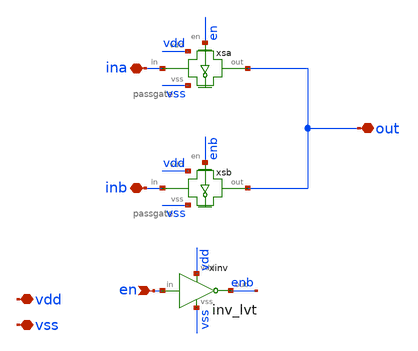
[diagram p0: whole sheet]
** sch_path: xschem/support/spdt.sch
**.subckt spdt en vss vdd ina out inb
*.ipin en
*.iopin vss
*.iopin vdd
*.iopin ina
*.iopin out
*.iopin inb
xinv vdd en enb vss inv_lvt
xsa out en vdd ina vss passgate
xsb out enb vdd inb vss passgate
**.ends

* expanding   symbol:  logic/inv_lvt.sym # of pins=4
** sym_path: xschem/logic/inv_lvt.sym
** sch_path: xschem/logic/inv_lvt.sch
.subckt inv_lvt vdd in out vss
*.iopin vdd
*.iopin vss
*.ipin in
*.opin out
XM1 out in vss vss sky130_fd_pr__nfet_01v8_lvt L=0.4 W=1 nf=1 ad='int((nf+1)/2) * W/nf * 0.29' as='int((nf+2)/2) * W/nf * 0.29'
+ pd='2*int((nf+1)/2) * (W/nf + 0.29)' ps='2*int((nf+2)/2) * (W/nf + 0.29)' nrd='0.29 / W' nrs='0.29 / W'
+ sa=0 sb=0 sd=0 mult=1 m=1
XM2 out in vdd vdd sky130_fd_pr__pfet_01v8_lvt L=0.4 W=1 nf=1 ad='int((nf+1)/2) * W/nf * 0.29' as='int((nf+2)/2) * W/nf * 0.29'
+ pd='2*int((nf+1)/2) * (W/nf + 0.29)' ps='2*int((nf+2)/2) * (W/nf + 0.29)' nrd='0.29 / W' nrs='0.29 / W'
+ sa=0 sb=0 sd=0 mult=1 m=1
.ends


* expanding   symbol:  switches/passgate.sym # of pins=5
** sym_path: xschem/switches/passgate.sym
** sch_path: xschem/switches/passgate.sch
.subckt passgate out en vdd in vss
*.iopin out
*.ipin en
*.iopin vss
*.iopin vdd
*.iopin in
x2 vdd en enb vss inv_lvt
x1 vdd enb en_buf vss inv_lvt
XMSN out en_buf in vss sky130_fd_pr__nfet_01v8 L=0.5 W=1 nf=1 ad='int((nf+1)/2) * W/nf * 0.29' as='int((nf+2)/2) * W/nf * 0.29'
+ pd='2*int((nf+1)/2) * (W/nf + 0.29)' ps='2*int((nf+2)/2) * (W/nf + 0.29)' nrd='0.29 / W' nrs='0.29 / W'
+ sa=0 sb=0 sd=0 mult=1 m=1
XMSP in enb out vdd sky130_fd_pr__pfet_01v8 L=0.5 W=1 nf=1 ad='int((nf+1)/2) * W/nf * 0.29' as='int((nf+2)/2) * W/nf * 0.29'
+ pd='2*int((nf+1)/2) * (W/nf + 0.29)' ps='2*int((nf+2)/2) * (W/nf + 0.29)' nrd='0.29 / W' nrs='0.29 / W'
+ sa=0 sb=0 sd=0 mult=1 m=1
.ends

.end
